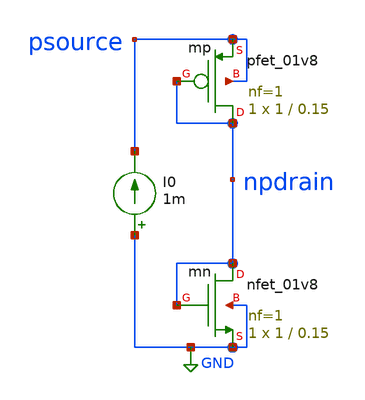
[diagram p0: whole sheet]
** sch_path: ISSCC25/submitted_notebooks/current_mirror_ota_optimization/characterization/sky130/schematics/cid_characterization_backup.sch
**.subckt cid_characterization_backup
xmn npdrain npdrain GND GND sky130_fd_pr__nfet_01v8 L=0.15 W=1 nf=1 ad='int((nf+1)/2) * W/nf * 0.29'
+ as='int((nf+2)/2) * W/nf * 0.29' pd='2*int((nf+1)/2) * (W/nf + 0.29)' ps='2*int((nf+2)/2) * (W/nf + 0.29)'
+ nrd='0.29 / W' nrs='0.29 / W' sa=0 sb=0 sd=0 mult=1 m=1
xmp npdrain npdrain psource psource sky130_fd_pr__pfet_01v8 L=0.15 W=1 nf=1 ad='int((nf+1)/2) * W/nf * 0.29'
+ as='int((nf+2)/2) * W/nf * 0.29' pd='2*int((nf+1)/2) * (W/nf + 0.29)' ps='2*int((nf+2)/2) * (W/nf + 0.29)'
+ nrd='0.29 / W' nrs='0.29 / W' sa=0 sb=0 sd=0 mult=1 m=1
I0 GND psource 1m
**** begin user architecture code



.lib /opt/pdk/open_pdks/sky130/sky130A/libs.tech/ngspice/sky130.lib.spice tt

.control


set filetype=ascii
set hcopydevtype=svg
save @m.xmn.msky130_fd_pr__nfet_01v8[gm]
save @m.xmn.msky130_fd_pr__nfet_01v8[id]
save @m.xmn.msky130_fd_pr__nfet_01v8[cgg]
save @m.xmn.msky130_fd_pr__nfet_01v8[cgs]
save @m.xmn.msky130_fd_pr__nfet_01v8[cgd]
save @m.xmn.msky130_fd_pr__nfet_01v8[cds]
save @m.xmn.msky130_fd_pr__nfet_01v8[css]
save @m.xmn.msky130_fd_pr__nfet_01v8[cdd]
save @m.xmn.msky130_fd_pr__nfet_01v8[gds]
save @m.xmn.msky130_fd_pr__nfet_01v8[vth]
save @m.xmn.msky130_fd_pr__nfet_01v8[vdsat]
save @m.xmn.msky130_fd_pr__nfet_01v8[vgs]
save @m.xmn.msky130_fd_pr__nfet_01v8[vds]

save @m.xmp.msky130_fd_pr__pfet_01v8[gm]
save @m.xmp.msky130_fd_pr__pfet_01v8[id]
save @m.xmp.msky130_fd_pr__pfet_01v8[cgg]
save @m.xmp.msky130_fd_pr__pfet_01v8[cgs]
save @m.xmp.msky130_fd_pr__pfet_01v8[cgd]
save @m.xmp.msky130_fd_pr__pfet_01v8[cds]
save @m.xmp.msky130_fd_pr__pfet_01v8[css]
save @m.xmp.msky130_fd_pr__pfet_01v8[cdd]
save @m.xmp.msky130_fd_pr__pfet_01v8[gds]
save @m.xmp.msky130_fd_pr__pfet_01v8[vth]
save @m.xmp.msky130_fd_pr__pfet_01v8[vdsat]
save @m.xmp.msky130_fd_pr__pfet_01v8[vgs]
save @m.xmp.msky130_fd_pr__pfet_01v8[vds]

dc I0 1u 10u 1u

let n_gm = @m.xmn.msky130_fd_pr__nfet_01v8[gm]
let n_id = @m.xmn.msky130_fd_pr__nfet_01v8[id]
let n_cgg = @m.xmn.msky130_fd_pr__nfet_01v8[cgg]
let n_cgs = @m.xmn.msky130_fd_pr__nfet_01v8[cgs]
let n_cgd = @m.xmn.msky130_fd_pr__nfet_01v8[cgd]
let n_cds = @m.xmn.msky130_fd_pr__nfet_01v8[cds]
let n_css = @m.xmn.msky130_fd_pr__nfet_01v8[css]
let n_cdd = @m.xmn.msky130_fd_pr__nfet_01v8[cdd]
let n_gds = @m.xmn.msky130_fd_pr__nfet_01v8[gds]
let n_vth = @m.xmn.msky130_fd_pr__nfet_01v8[vth]
let n_vdsat = @m.xmn.msky130_fd_pr__nfet_01v8[vdsat]
let n_vgs = @m.xmn.msky130_fd_pr__nfet_01v8[vgs]
let n_vds = @m.xmn.msky130_fd_pr__nfet_01v8[vds]

let p_gm = @m.xmp.msky130_fd_pr__pfet_01v8[gm]
let p_id = @m.xmp.msky130_fd_pr__pfet_01v8[id]
let p_cgg = @m.xmp.msky130_fd_pr__pfet_01v8[cgg]
let p_cgs = @m.xmp.msky130_fd_pr__pfet_01v8[cgs]
let p_cgd = @m.xmp.msky130_fd_pr__pfet_01v8[cgd]
let p_cds = @m.xmp.msky130_fd_pr__pfet_01v8[cds]
let p_css = @m.xmp.msky130_fd_pr__pfet_01v8[css]
let p_cdd = @m.xmp.msky130_fd_pr__pfet_01v8[cdd]
let p_gds = @m.xmp.msky130_fd_pr__pfet_01v8[gds]
let p_vth = @m.xmp.msky130_fd_pr__pfet_01v8[vth]
let p_vdsat = @m.xmp.msky130_fd_pr__pfet_01v8[vdsat]
let p_vgs = @m.xmp.msky130_fd_pr__pfet_01v8[vgs]
let p_vds = @m.xmp.msky130_fd_pr__pfet_01v8[vds]

let n_rds = 1/n_gds
let n_wt = n_gm/n_cgg
let n_ft = n_wt/(2*pi)
let n_gm_id = n_gm/n_id

let p_rds = 1/p_gds
let p_wt = p_gm/p_cgg
let p_ft = p_wt/(2*pi)
let p_gm_id = p_gm/p_id

**let gm_id = gm/id
**let ft_n = @mn[gm]/@mn[cgg]
**let gm_id_n = @xmn[gm]/@xmn[id]
write nfet_cid_characterization.txt n_gm n_id n_cgg n_cgs n_cgd n_cds n_css n_cdd n_gds n_vth
+ n_vdsat n_vgs n_vds n_rds n_wt n_ft n_gm_id
write pfet_cid_characterization.txt p_gm p_id p_cgg p_cgs p_cgd p_cds p_css p_cdd p_gds p_vth
+ p_vdsat p_vgs p_vds p_rds p_wt p_ft p_gm_id

**plot ft_n vs gm_id_n ylog


.endc


.save all



**** end user architecture code
**.ends
.GLOBAL GND
.end
